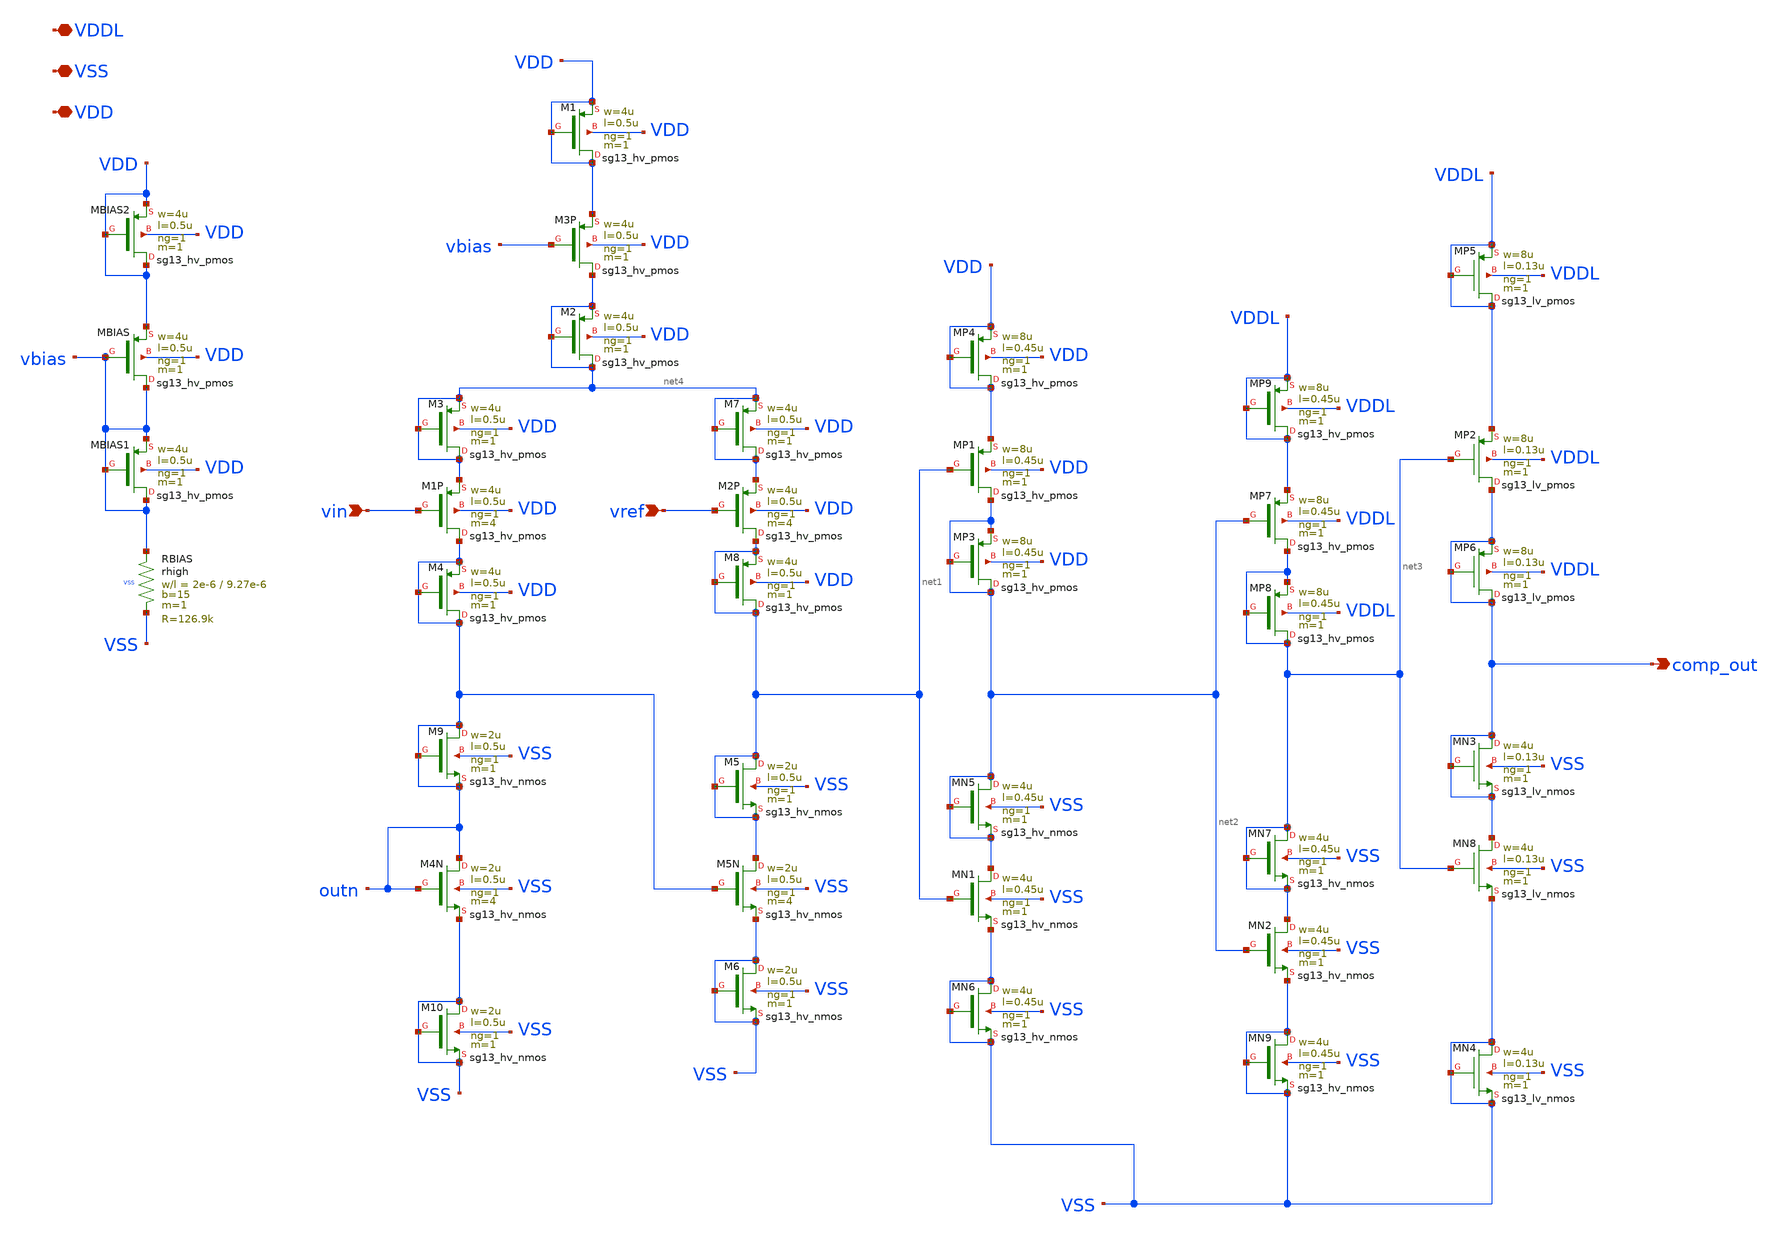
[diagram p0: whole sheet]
** sch_path: macros/heichips26_ook_top/macros/ook_analog_system/schematic/xschem/simple_comparator.sch
**.subckt simple_comparator vin vref VDD VSS comp_out VDDL
*.ipin vin
*.ipin vref
*.iopin VDD
*.iopin VSS
*.opin comp_out
*.iopin VDDL
XMBIAS vbias vbias VDD VDD sg13_hv_pmos w=4u l=0.5u ng=1 m=1 mm_ok=1
XRBIAS vbias VSS VSS rhigh w=2e-6 l=9.27e-6 m=1 b=15 ps=0.18e-6 mm_ok=1
XM3P net4 vbias VDD VDD sg13_hv_pmos w=4u l=0.5u ng=1 m=1 mm_ok=1
XM1P outn vin net4 VDD sg13_hv_pmos w=4u l=0.5u ng=1 m=4 mm_ok=1
XM2P net1 vref net4 VDD sg13_hv_pmos w=4u l=0.5u ng=1 m=4 mm_ok=1
XM4N outn outn VSS VSS sg13_hv_nmos w=2u l=0.5u ng=1 m=4 mm_ok=1
XM5N net1 outn VSS VSS sg13_hv_nmos w=2u l=0.5u ng=1 m=4 mm_ok=1
XMP1 net2 net1 VDD VDD sg13_hv_pmos w=8u l=0.45u ng=1 m=1 mm_ok=1
XMN1 net2 net1 VSS VSS sg13_hv_nmos w=4u l=0.45u ng=1 m=1 mm_ok=1
XMP2 comp_out net3 VDDL VDDL sg13_lv_pmos w=8u l=0.13u ng=1 m=1 mm_ok=1
XMBIAS1 vbias vbias vbias VDD sg13_hv_pmos w=4u l=0.5u ng=1 m=1 mm_ok=1
XMBIAS2 VDD VDD VDD VDD sg13_hv_pmos w=4u l=0.5u ng=1 m=1 mm_ok=1
XM1 VDD VDD VDD VDD sg13_hv_pmos w=4u l=0.5u ng=1 m=1 mm_ok=1
XM2 net4 net4 net4 VDD sg13_hv_pmos w=4u l=0.5u ng=1 m=1 mm_ok=1
XMP3 net2 net2 net2 VDD sg13_hv_pmos w=8u l=0.45u ng=1 m=1 mm_ok=1
XMP4 VDD VDD VDD VDD sg13_hv_pmos w=8u l=0.45u ng=1 m=1 mm_ok=1
XMP5 VDDL VDDL VDDL VDDL sg13_lv_pmos w=8u l=0.13u ng=1 m=1 mm_ok=1
XMP6 comp_out comp_out comp_out VDDL sg13_lv_pmos w=8u l=0.13u ng=1 m=1 mm_ok=1
XMN3 comp_out comp_out comp_out VSS sg13_lv_nmos w=4u l=0.13u ng=1 m=1 mm_ok=1
XMN4 VSS VSS VSS VSS sg13_lv_nmos w=4u l=0.13u ng=1 m=1 mm_ok=1
XMN5 net2 net2 net2 VSS sg13_hv_nmos w=4u l=0.45u ng=1 m=1 mm_ok=1
XMN6 VSS VSS VSS VSS sg13_hv_nmos w=4u l=0.45u ng=1 m=1 mm_ok=1
XM3 net4 net4 net4 VDD sg13_hv_pmos w=4u l=0.5u ng=1 m=1 mm_ok=1
XM4 outn outn outn VDD sg13_hv_pmos w=4u l=0.5u ng=1 m=1 mm_ok=1
XM5 net1 net1 net1 VSS sg13_hv_nmos w=2u l=0.5u ng=1 m=1 mm_ok=1
XM6 VSS VSS VSS VSS sg13_hv_nmos w=2u l=0.5u ng=1 m=1 mm_ok=1
XM7 net4 net4 net4 VDD sg13_hv_pmos w=4u l=0.5u ng=1 m=1 mm_ok=1
XM8 net1 net1 net1 VDD sg13_hv_pmos w=4u l=0.5u ng=1 m=1 mm_ok=1
XM9 outn outn outn VSS sg13_hv_nmos w=2u l=0.5u ng=1 m=1 mm_ok=1
XM10 VSS VSS VSS VSS sg13_hv_nmos w=2u l=0.5u ng=1 m=1 mm_ok=1
XMN8 comp_out net3 VSS VSS sg13_lv_nmos w=4u l=0.13u ng=1 m=1 mm_ok=1
XMP7 net3 net2 VDDL VDDL sg13_hv_pmos w=8u l=0.45u ng=1 m=1 mm_ok=1
XMN2 net3 net2 VSS VSS sg13_hv_nmos w=4u l=0.45u ng=1 m=1 mm_ok=1
XMP8 net3 net3 net3 VDDL sg13_hv_pmos w=8u l=0.45u ng=1 m=1 mm_ok=1
XMP9 VDDL VDDL VDDL VDDL sg13_hv_pmos w=8u l=0.45u ng=1 m=1 mm_ok=1
XMN7 net3 net3 net3 VSS sg13_hv_nmos w=4u l=0.45u ng=1 m=1 mm_ok=1
XMN9 VSS VSS VSS VSS sg13_hv_nmos w=4u l=0.45u ng=1 m=1 mm_ok=1
**.ends
.end
